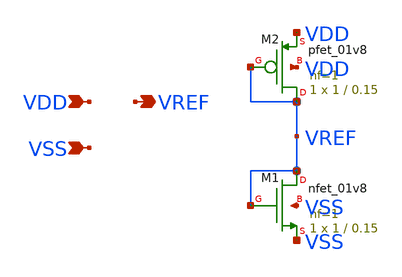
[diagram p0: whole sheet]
** sch_path: week4/xschem/adc/ladder.sch
**.subckt ladder VREF VSS VDD
*.opin VREF
*.ipin VSS
*.ipin VDD
XM1 VREF VREF VSS VSS sky130_fd_pr__nfet_01v8 L=0.15 W=1 nf=1 ad='int((nf+1)/2) * W/nf * 0.29' as='int((nf+2)/2) * W/nf * 0.29'
+ pd='2*int((nf+1)/2) * (W/nf + 0.29)' ps='2*int((nf+2)/2) * (W/nf + 0.29)' nrd='0.29 / W' nrs='0.29 / W'
+ sa=0 sb=0 sd=0 mult=1 m=1
XM2 VREF VREF VDD VDD sky130_fd_pr__pfet_01v8 L=0.15 W=1 nf=1 ad='int((nf+1)/2) * W/nf * 0.29' as='int((nf+2)/2) * W/nf * 0.29'
+ pd='2*int((nf+1)/2) * (W/nf + 0.29)' ps='2*int((nf+2)/2) * (W/nf + 0.29)' nrd='0.29 / W' nrs='0.29 / W'
+ sa=0 sb=0 sd=0 mult=1 m=1
**.ends
.end
